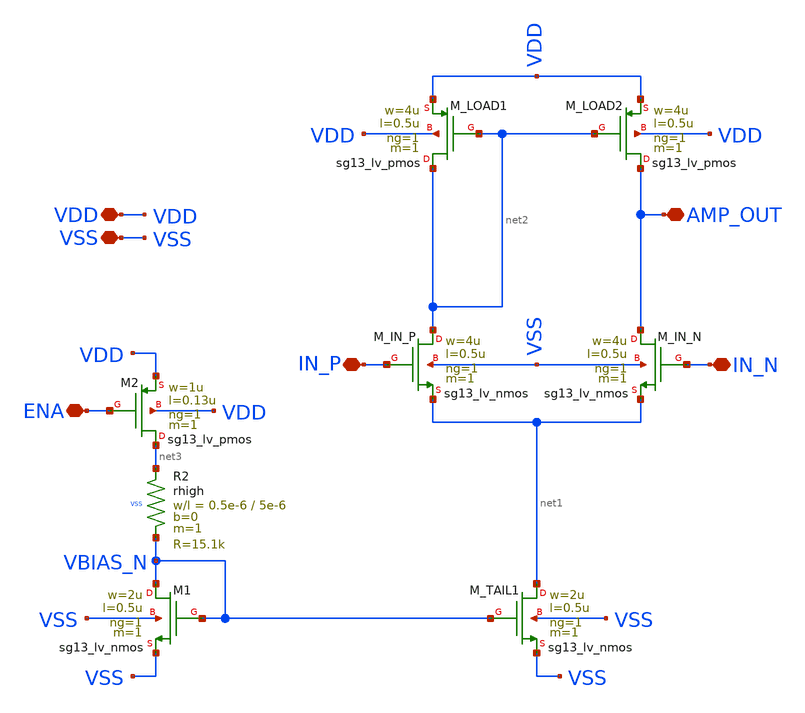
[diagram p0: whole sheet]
** sch_path: xschem/Simple_OTA.sch
**.subckt Simple_OTA VDD IN_N IN_P AMP_OUT VSS ENA
*.iopin VDD
*.iopin IN_N
*.iopin IN_P
*.iopin AMP_OUT
*.iopin VSS
*.iopin ENA
XM_LOAD1 net2 net2 VDD VDD sg13_lv_pmos w=4u l=0.5u ng=1 m=1 mm_ok=1
XM_IN_P net2 IN_P net1 VSS sg13_lv_nmos w=4u l=0.5u ng=1 m=1 mm_ok=1
XM_IN_N AMP_OUT IN_N net1 VSS sg13_lv_nmos w=4u l=0.5u ng=1 m=1 mm_ok=1
XM_LOAD2 AMP_OUT net2 VDD VDD sg13_lv_pmos w=4u l=0.5u ng=1 m=1 mm_ok=1
XM1 VBIAS_N VBIAS_N VSS VSS sg13_lv_nmos w=2u l=0.5u ng=1 m=1 mm_ok=1
XR2 net3 VBIAS_N VSS rhigh w=0.5e-6 l=5e-6 m=1 b=0 mm_ok=1
XM_TAIL1 net1 VBIAS_N VSS VSS sg13_lv_nmos w=2u l=0.5u ng=1 m=1 mm_ok=1
XM2 net3 ENA VDD VDD sg13_lv_pmos w=1u l=0.13u ng=1 m=1 mm_ok=1
**.ends
.end
